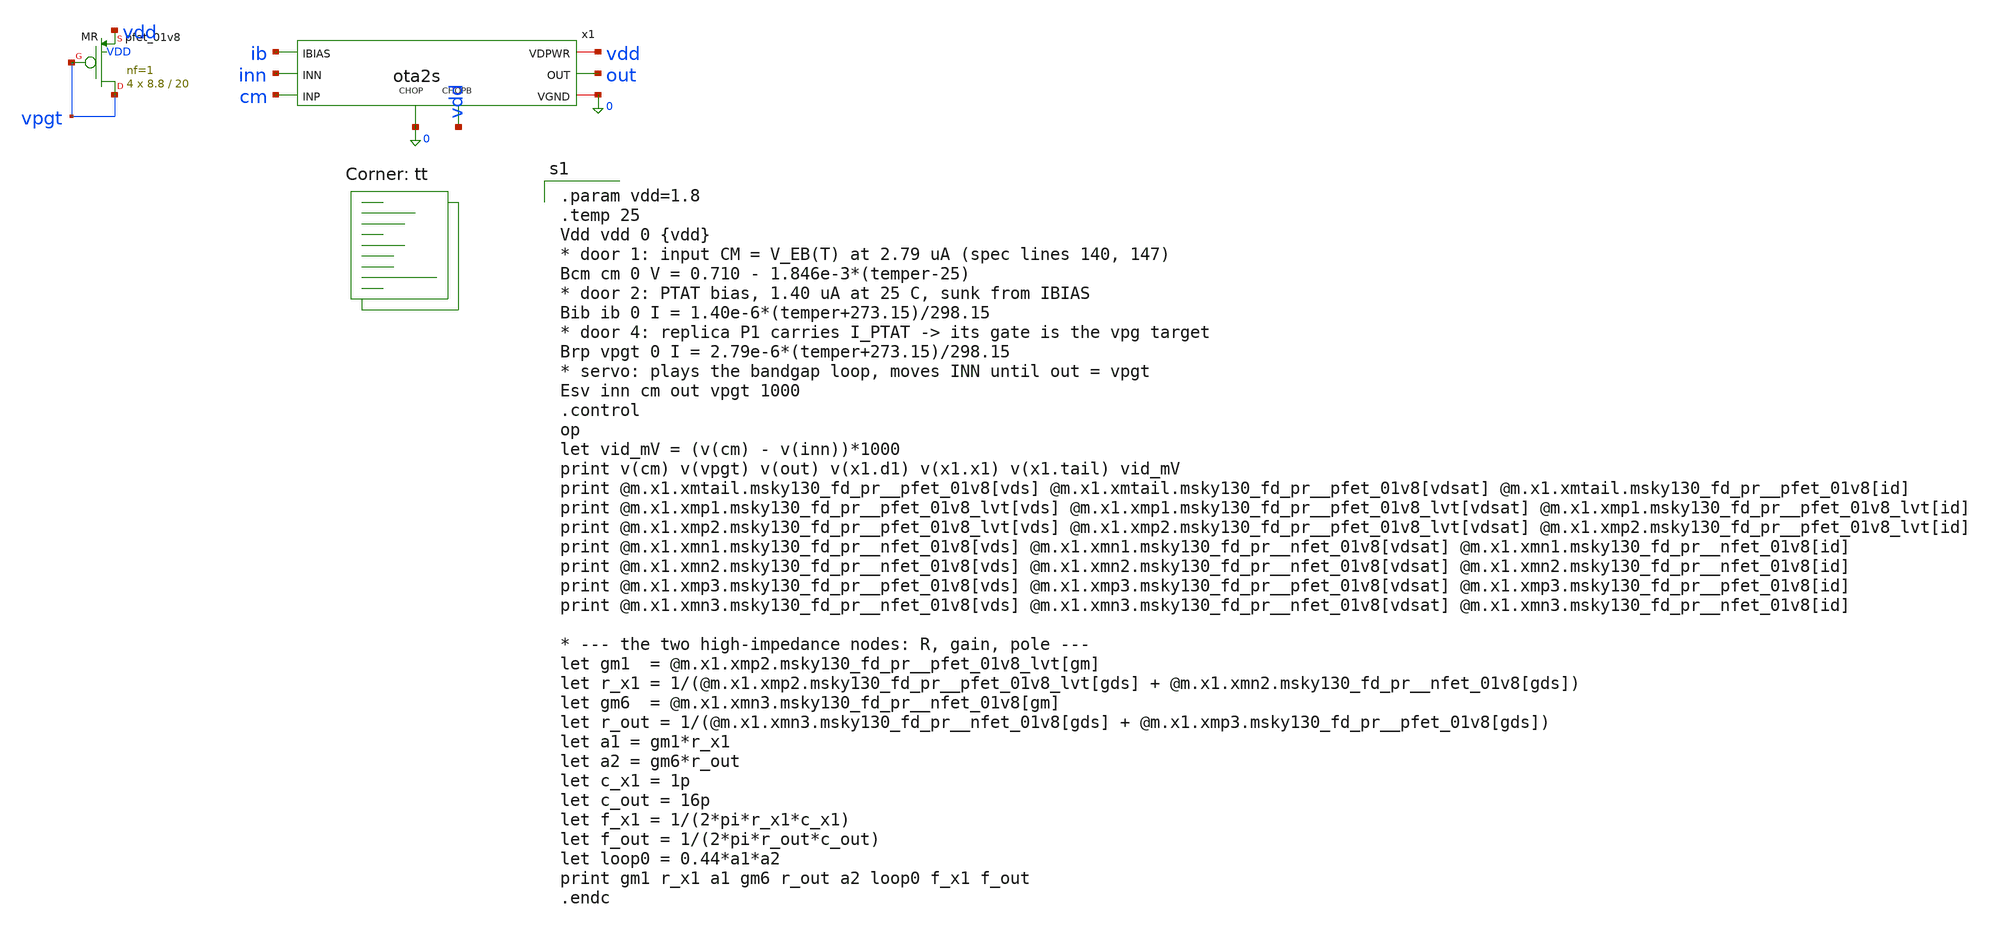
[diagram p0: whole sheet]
** sch_path: xschem/tb_ota2s_op.sch
**.subckt tb_ota2s_op
x1 cm inn out vdd 0 ib 0 vdd ota2s
XMR vpgt vpgt vdd VDD sky130_fd_pr__pfet_01v8 L=20 W=8.8 nf=1 ad='int((1 + 1)/2) * 8.8 / 1 * 0.29' as='int((1 + 2)/2) * 8.8 / 1 * 0.29'
+ pd='2*int((1 + 1)/2) * (8.8 / 1 + 0.29)' ps='2*int((1 + 2)/2) * (8.8 / 1 + 0.29)' nrd='0.29 / 8.8 ' nrs='0.29 / 8.8 '
+ sa=0 sb=0 sd=0 mult=4 m=4
**** begin user architecture code
.lib $::SKYWATER_MODELS/sky130.lib.spice tt

.param vdd=1.8
.temp 25
Vdd vdd 0 {vdd}
* door 1: input CM = V_EB(T) at 2.79 uA (spec lines 140, 147)
Bcm cm 0 V = 0.710 - 1.846e-3*(temper-25)
* door 2: PTAT bias, 1.40 uA at 25 C, sunk from IBIAS
Bib ib 0 I = 1.40e-6*(temper+273.15)/298.15
* door 4: replica P1 carries I_PTAT -> its gate is the vpg target
Brp vpgt 0 I = 2.79e-6*(temper+273.15)/298.15
* servo: plays the bandgap loop, moves INN until out = vpgt
Esv inn cm out vpgt 1000
.control
op
let vid_mV = (v(cm) - v(inn))*1000
print v(cm) v(vpgt) v(out) v(x1.d1) v(x1.x1) v(x1.tail) vid_mV
print @m.x1.xmtail.msky130_fd_pr__pfet_01v8[vds] @m.x1.xmtail.msky130_fd_pr__pfet_01v8[vdsat]
+ @m.x1.xmtail.msky130_fd_pr__pfet_01v8[id]
print @m.x1.xmp1.msky130_fd_pr__pfet_01v8_lvt[vds] @m.x1.xmp1.msky130_fd_pr__pfet_01v8_lvt[vdsat]
+ @m.x1.xmp1.msky130_fd_pr__pfet_01v8_lvt[id]
print @m.x1.xmp2.msky130_fd_pr__pfet_01v8_lvt[vds] @m.x1.xmp2.msky130_fd_pr__pfet_01v8_lvt[vdsat]
+ @m.x1.xmp2.msky130_fd_pr__pfet_01v8_lvt[id]
print @m.x1.xmn1.msky130_fd_pr__nfet_01v8[vds] @m.x1.xmn1.msky130_fd_pr__nfet_01v8[vdsat]
+ @m.x1.xmn1.msky130_fd_pr__nfet_01v8[id]
print @m.x1.xmn2.msky130_fd_pr__nfet_01v8[vds] @m.x1.xmn2.msky130_fd_pr__nfet_01v8[vdsat]
+ @m.x1.xmn2.msky130_fd_pr__nfet_01v8[id]
print @m.x1.xmp3.msky130_fd_pr__pfet_01v8[vds] @m.x1.xmp3.msky130_fd_pr__pfet_01v8[vdsat]
+ @m.x1.xmp3.msky130_fd_pr__pfet_01v8[id]
print @m.x1.xmn3.msky130_fd_pr__nfet_01v8[vds] @m.x1.xmn3.msky130_fd_pr__nfet_01v8[vdsat]
+ @m.x1.xmn3.msky130_fd_pr__nfet_01v8[id]

* --- the two high-impedance nodes: R, gain, pole ---
let gm1  = @m.x1.xmp2.msky130_fd_pr__pfet_01v8_lvt[gm]
let r_x1 = 1/(@m.x1.xmp2.msky130_fd_pr__pfet_01v8_lvt[gds] +
+ @m.x1.xmn2.msky130_fd_pr__nfet_01v8[gds])
let gm6  = @m.x1.xmn3.msky130_fd_pr__nfet_01v8[gm]
let r_out = 1/(@m.x1.xmn3.msky130_fd_pr__nfet_01v8[gds] + @m.x1.xmp3.msky130_fd_pr__pfet_01v8[gds])
let a1 = gm1*r_x1
let a2 = gm6*r_out
let c_x1 = 1p
let c_out = 16p
let f_x1 = 1/(2*pi*r_x1*c_x1)
let f_out = 1/(2*pi*r_out*c_out)
let loop0 = 0.44*a1*a2
print gm1 r_x1 a1 gm6 r_out a2 loop0 f_x1 f_out
.endc

**** end user architecture code
**.ends

* expanding   symbol:  ota2s.sym # of pins=8
** sym_path: xschem/ota2s.sym
** sch_path: xschem/ota2s.sch
.subckt ota2s INP INN OUT VDPWR VGND IBIAS CHOP CHOPB
*.ipin INN
*.ipin INP
*.ipin IBIAS
*.opin OUT
*.iopin VDPWR
*.iopin VGND
*.ipin CHOPB
*.ipin CHOP
XMREF IBIAS IBIAS VDPWR VDPWR sky130_fd_pr__pfet_01v8 L=4 W=20 nf=1 ad='int((1 + 1)/2) * 20 / 1 * 0.29'
+ as='int((1 + 2)/2) * 20 / 1 * 0.29' pd='2*int((1 + 1)/2) * (20 / 1 + 0.29)' ps='2*int((1 + 2)/2) * (20 / 1 + 0.29)'
+ nrd='0.29 / 20 ' nrs='0.29 / 20 ' sa=0 sb=0 sd=0 mult=1 m=1
XMTAIL tail IBIAS VDPWR VDPWR sky130_fd_pr__pfet_01v8 L=4 W=20 nf=1 ad='int((1 + 1)/2) * 20 / 1 * 0.29'
+ as='int((1 + 2)/2) * 20 / 1 * 0.29' pd='2*int((1 + 1)/2) * (20 / 1 + 0.29)' ps='2*int((1 + 2)/2) * (20 / 1 + 0.29)'
+ nrd='0.29 / 20 ' nrs='0.29 / 20 ' sa=0 sb=0 sd=0 mult=2 m=2
XMP1 d1 INN tail VDPWR sky130_fd_pr__pfet_01v8_lvt L=6 W=25 nf=1 ad='int((1 + 1)/2) * 25 / 1 * 0.29'
+ as='int((1 + 2)/2) * 25 / 1 * 0.29' pd='2*int((1 + 1)/2) * (25 / 1 + 0.29)' ps='2*int((1 + 2)/2) * (25 / 1 + 0.29)'
+ nrd='0.29 / 25 ' nrs='0.29 / 25 ' sa=0 sb=0 sd=0 mult=24 m=24
XMP2 x1 INP tail VDPWR sky130_fd_pr__pfet_01v8_lvt L=6 W=25 nf=1 ad='int((1 + 1)/2) * 25 / 1 * 0.29'
+ as='int((1 + 2)/2) * 25 / 1 * 0.29' pd='2*int((1 + 1)/2) * (25 / 1 + 0.29)' ps='2*int((1 + 2)/2) * (25 / 1 + 0.29)'
+ nrd='0.29 / 25 ' nrs='0.29 / 25 ' sa=0 sb=0 sd=0 mult=24 m=24
XMN1 d1 g12 VGND VGND sky130_fd_pr__nfet_01v8 L=20 W=6 nf=1 ad='int((1 + 1)/2) * 6 / 1 * 0.29' as='int((1 + 2)/2) * 6 / 1 * 0.29'
+ pd='2*int((1 + 1)/2) * (6 / 1 + 0.29)' ps='2*int((1 + 2)/2) * (6 / 1 + 0.29)' nrd='0.29 / 6 ' nrs='0.29 / 6 '
+ sa=0 sb=0 sd=0 mult=2 m=2
XMN2 x1 g12 VGND VGND sky130_fd_pr__nfet_01v8 L=20 W=6 nf=1 ad='int((1 + 1)/2) * 6 / 1 * 0.29' as='int((1 + 2)/2) * 6 / 1 * 0.29'
+ pd='2*int((1 + 1)/2) * (6 / 1 + 0.29)' ps='2*int((1 + 2)/2) * (6 / 1 + 0.29)' nrd='0.29 / 6 ' nrs='0.29 / 6 '
+ sa=0 sb=0 sd=0 mult=2 m=2
XMP3 OUT IBIAS VDPWR VDPWR sky130_fd_pr__pfet_01v8 L=4 W=20 nf=1 ad='int((1 + 1)/2) * 20 / 1 * 0.29'
+ as='int((1 + 2)/2) * 20 / 1 * 0.29' pd='2*int((1 + 1)/2) * (20 / 1 + 0.29)' ps='2*int((1 + 2)/2) * (20 / 1 + 0.29)'
+ nrd='0.29 / 20 ' nrs='0.29 / 20 ' sa=0 sb=0 sd=0 mult=6 m=6
XMN3 OUT g3 VGND VGND sky130_fd_pr__nfet_01v8 L=1 W=7 nf=1 ad='int((1 + 1)/2) * 7 / 1 * 0.29' as='int((1 + 2)/2) * 7 / 1 * 0.29'
+ pd='2*int((1 + 1)/2) * (7 / 1 + 0.29)' ps='2*int((1 + 2)/2) * (7 / 1 + 0.29)' nrd='0.29 / 7 ' nrs='0.29 / 7 '
+ sa=0 sb=0 sd=0 mult=1 m=1
XRZ1 net1 g3 VGND sky130_fd_pr__res_high_po_1p41 L=20 mult=1 m=1
XRZ2 net2 net1 VGND sky130_fd_pr__res_high_po_1p41 L=20 mult=1 m=1
XRZ3 net3 net2 VGND sky130_fd_pr__res_high_po_1p41 L=20 mult=1 m=1
XRZ4 net4 net3 VGND sky130_fd_pr__res_high_po_1p41 L=20 mult=1 m=1
XRZ5 net5 net4 VGND sky130_fd_pr__res_high_po_1p41 L=20 mult=1 m=1
XRZ6 cz net5 VGND sky130_fd_pr__res_high_po_1p41 L=20 mult=1 m=1
XCC cz OUT sky130_fd_pr__cap_mim_m3_1 W=25 L=25 MF=8 m=8
XDP tail VDPWR tail VDPWR sky130_fd_pr__pfet_01v8_lvt L=6 W=25 nf=1 ad='int((1 + 1)/2) * 25 / 1 * 0.29'
+ as='int((1 + 2)/2) * 25 / 1 * 0.29' pd='2*int((1 + 1)/2) * (25 / 1 + 0.29)' ps='2*int((1 + 2)/2) * (25 / 1 + 0.29)'
+ nrd='0.29 / 25 ' nrs='0.29 / 25 ' sa=0 sb=0 sd=0 mult=8 m=8
XDNA d1 VGND VGND VGND sky130_fd_pr__nfet_01v8 L=20 W=6 nf=1 ad='int((1 + 1)/2) * 6 / 1 * 0.29' as='int((1 + 2)/2) * 6 / 1 * 0.29'
+ pd='2*int((1 + 1)/2) * (6 / 1 + 0.29)' ps='2*int((1 + 2)/2) * (6 / 1 + 0.29)' nrd='0.29 / 6 ' nrs='0.29 / 6 '
+ sa=0 sb=0 sd=0 mult=2 m=2
XDNB x1 VGND VGND VGND sky130_fd_pr__nfet_01v8 L=20 W=6 nf=1 ad='int((1 + 1)/2) * 6 / 1 * 0.29' as='int((1 + 2)/2) * 6 / 1 * 0.29'
+ pd='2*int((1 + 1)/2) * (6 / 1 + 0.29)' ps='2*int((1 + 2)/2) * (6 / 1 + 0.29)' nrd='0.29 / 6 ' nrs='0.29 / 6 '
+ sa=0 sb=0 sd=0 mult=2 m=2
XDB VDPWR VDPWR VDPWR VDPWR sky130_fd_pr__pfet_01v8 L=4 W=20 nf=1 ad='int((1 + 1)/2) * 20 / 1 * 0.29'
+ as='int((1 + 2)/2) * 20 / 1 * 0.29' pd='2*int((1 + 1)/2) * (20 / 1 + 0.29)' ps='2*int((1 + 2)/2) * (20 / 1 + 0.29)'
+ nrd='0.29 / 20 ' nrs='0.29 / 20 ' sa=0 sb=0 sd=0 mult=2 m=2
XRD1 VGND VGND VGND sky130_fd_pr__res_high_po_1p41 L=20 mult=1 m=1
XRD2 VGND VGND VGND sky130_fd_pr__res_high_po_1p41 L=20 mult=1 m=1
XSD1 d1 CHOPB g12 VGND sky130_fd_pr__nfet_01v8 L=0.5 W=6 nf=1 ad='int((1 + 1)/2) * 6 / 1 * 0.29' as='int((1 + 2)/2) * 6 / 1 * 0.29'
+ pd='2*int((1 + 1)/2) * (6 / 1 + 0.29)' ps='2*int((1 + 2)/2) * (6 / 1 + 0.29)' nrd='0.29 / 6 ' nrs='0.29 / 6 '
+ sa=0 sb=0 sd=0 mult=1 m=1
XSD2 x1 CHOP g12 VGND sky130_fd_pr__nfet_01v8 L=0.5 W=6 nf=1 ad='int((1 + 1)/2) * 6 / 1 * 0.29' as='int((1 + 2)/2) * 6 / 1 * 0.29'
+ pd='2*int((1 + 1)/2) * (6 / 1 + 0.29)' ps='2*int((1 + 2)/2) * (6 / 1 + 0.29)' nrd='0.29 / 6 ' nrs='0.29 / 6 '
+ sa=0 sb=0 sd=0 mult=1 m=1
XSG2 g3 CHOP d1 VGND sky130_fd_pr__nfet_01v8 L=0.5 W=6 nf=1 ad='int((1 + 1)/2) * 6 / 1 * 0.29' as='int((1 + 2)/2) * 6 / 1 * 0.29'
+ pd='2*int((1 + 1)/2) * (6 / 1 + 0.29)' ps='2*int((1 + 2)/2) * (6 / 1 + 0.29)' nrd='0.29 / 6 ' nrs='0.29 / 6 '
+ sa=0 sb=0 sd=0 mult=1 m=1
XSG1 x1 CHOPB g3 VGND sky130_fd_pr__nfet_01v8 L=0.5 W=6 nf=1 ad='int((1 + 1)/2) * 6 / 1 * 0.29' as='int((1 + 2)/2) * 6 / 1 * 0.29'
+ pd='2*int((1 + 1)/2) * (6 / 1 + 0.29)' ps='2*int((1 + 2)/2) * (6 / 1 + 0.29)' nrd='0.29 / 6 ' nrs='0.29 / 6 '
+ sa=0 sb=0 sd=0 mult=1 m=1
.ends

.end
